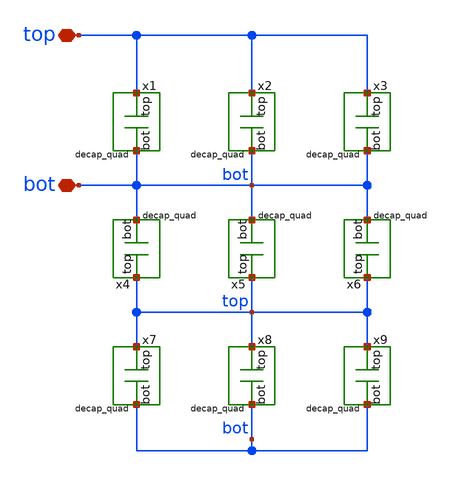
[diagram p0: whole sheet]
** sch_path: v2_feature_extr_withf/decap_unit_bottom.sch
**.subckt decap_unit_bottom top bot
*.iopin top
*.iopin bot
x1 top bot decap_quad
x2 top bot decap_quad
x3 top bot decap_quad
x4 top bot decap_quad
x5 top bot decap_quad
x6 top bot decap_quad
x7 top bot decap_quad
x8 top bot decap_quad
x9 top bot decap_quad
**.ends
.end
